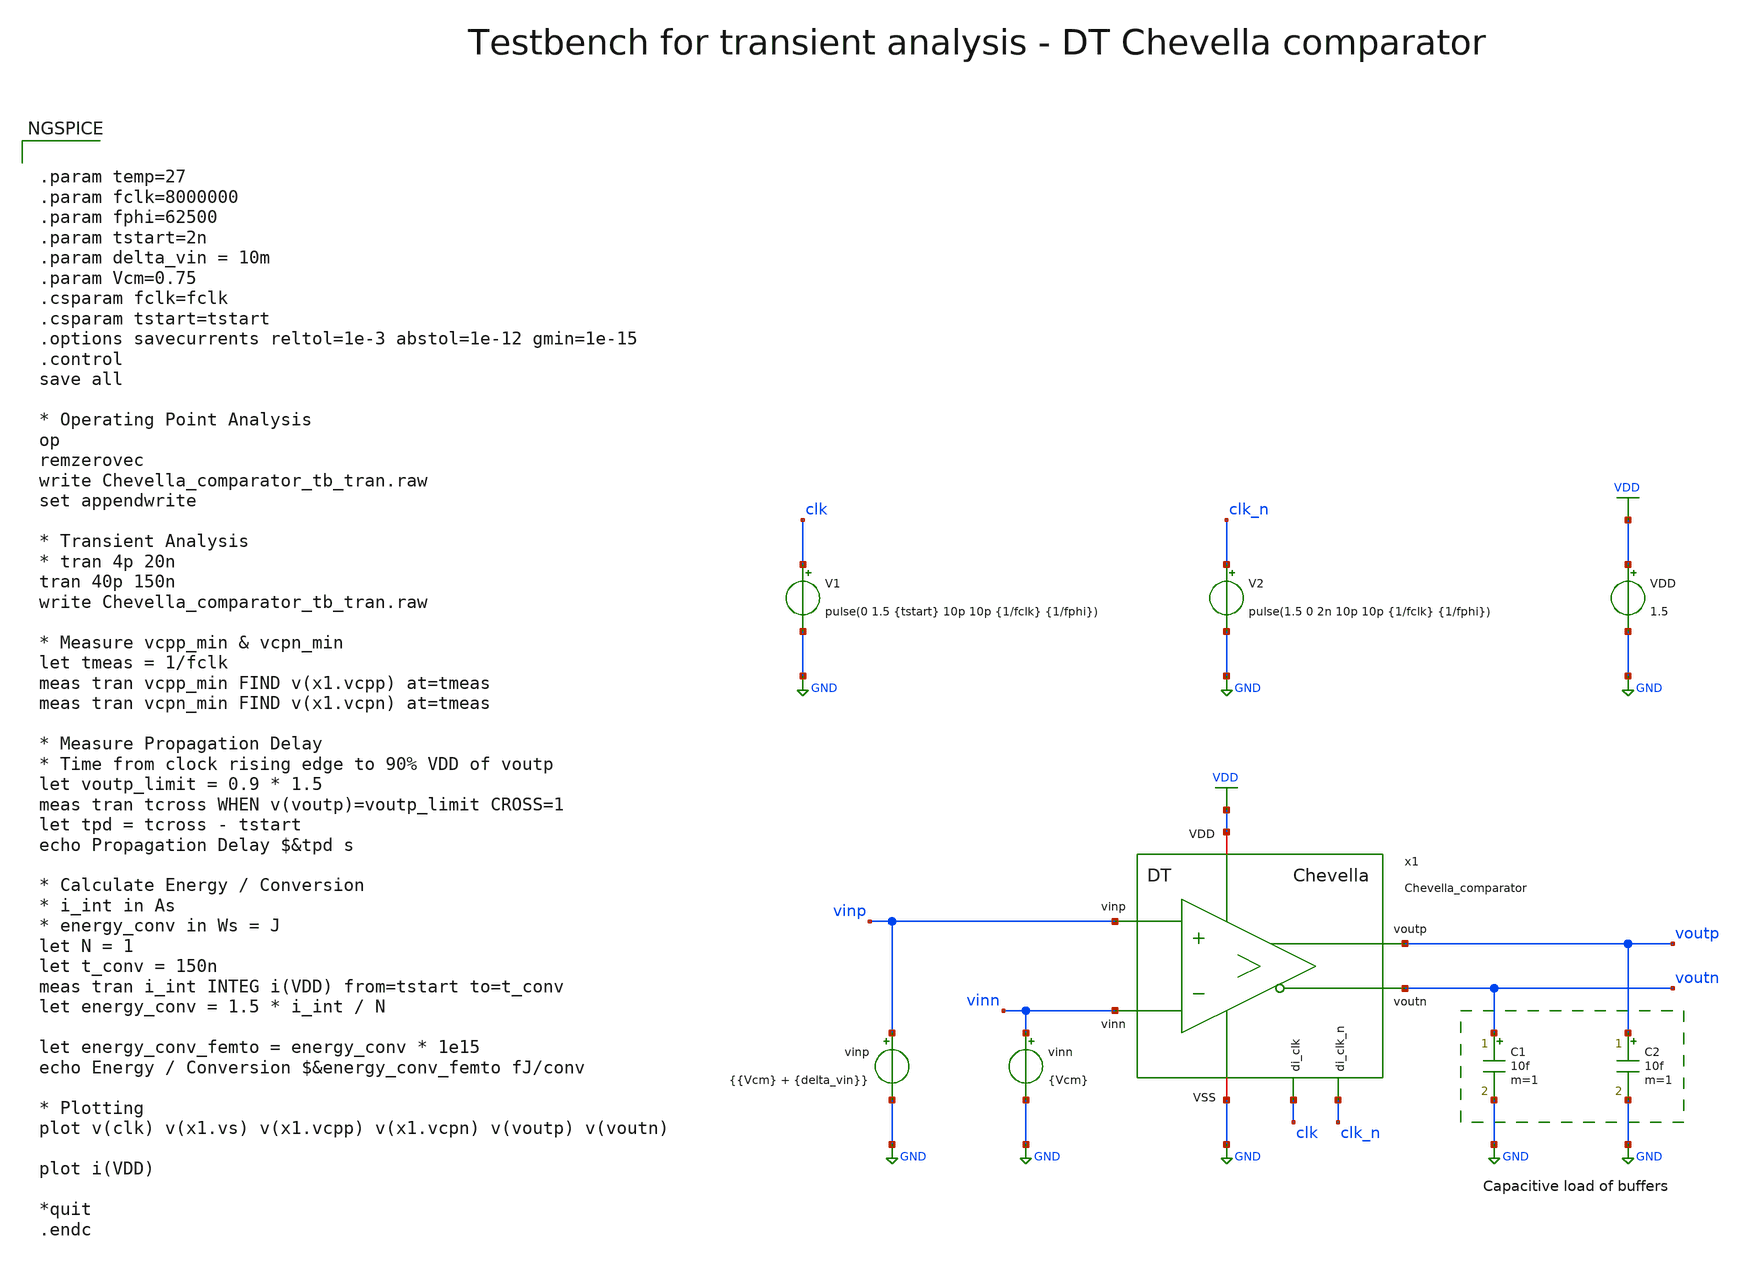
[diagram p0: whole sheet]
** sch_path: SG13G2_ATBS-ADC-main/xschem/comparator/discrete_time/Chevella/testbenches/Chevella_comparator_tb_tran.sch
**.subckt Chevella_comparator_tb_tran
VDD VDD GND 1.5
V1 clk GND pulse(0 1.5 {tstart} 10p 10p {1/fclk} {1/fphi})
vinn vinn GND {Vcm}
vinp vinp GND {{Vcm} + {delta_vin}}
V2 clk_n GND pulse(1.5 0 2n 10p 10p {1/fclk} {1/fphi})
C1 voutn GND 10f m=1
C2 voutp GND 10f m=1
x1 clk_n clk VDD voutp vinp GND voutn vinn Chevella_comparator
**** begin user architecture code

.lib cornerMOSlv.lib mos_tt
.lib cornerMOShv.lib mos_tt
.lib cornerRES.lib res_typ



.param temp=27
.param fclk=8000000
.param fphi=62500
.param tstart=2n
.param delta_vin = 10m
.param Vcm=0.75
.csparam fclk=fclk
.csparam tstart=tstart
.options savecurrents reltol=1e-3 abstol=1e-12 gmin=1e-15
.control
save all

* Operating Point Analysis
op
remzerovec
write Chevella_comparator_tb_tran.raw
set appendwrite

* Transient Analysis
* tran 4p 20n
tran 40p 150n
write Chevella_comparator_tb_tran.raw

* Measure vcpp_min & vcpn_min
let tmeas = 1/fclk
meas tran vcpp_min FIND v(x1.vcpp) at=tmeas
meas tran vcpn_min FIND v(x1.vcpn) at=tmeas

* Measure Propagation Delay
* Time from clock rising edge to 90% VDD of voutp
let voutp_limit = 0.9 * 1.5
meas tran tcross WHEN v(voutp)=voutp_limit CROSS=1
let tpd = tcross - tstart
echo Propagation Delay $&tpd s

* Calculate Energy / Conversion
* i_int in As
* energy_conv in Ws = J
let N = 1
let t_conv = 150n
meas tran i_int INTEG i(VDD) from=tstart to=t_conv
let energy_conv = 1.5 * i_int / N

let energy_conv_femto = energy_conv * 1e15
echo Energy / Conversion $&energy_conv_femto fJ/conv

* Plotting
plot v(clk) v(x1.vs) v(x1.vcpp) v(x1.vcpn) v(voutp) v(voutn)

plot i(VDD)

*quit
.endc

**** end user architecture code
**.ends

* expanding   symbol:  comparator/discrete_time/Chevella/Chevella_comparator.sym # of pins=8
** sym_path: SG13G2_ATBS-ADC-main/xschem/comparator/discrete_time/Chevella/Chevella_comparator.sym
** sch_path: SG13G2_ATBS-ADC-main/xschem/comparator/discrete_time/Chevella/Chevella_comparator.sch
.subckt Chevella_comparator di_clk_n di_clk VDD voutp vinp VSS voutn vinn
*.iopin VDD
*.opin voutp
*.opin voutn
*.ipin di_clk_n
*.iopin VSS
*.ipin vinp
*.ipin vinn
*.ipin di_clk
XM1a vcpn vinp net1 VSS sg13_lv_nmos w=1.0u l=0.13u ng=1 m=1 mm_ok=1
XM2a vcpp vinn net2 VSS sg13_lv_nmos w=1.0u l=0.13u ng=1 m=1 mm_ok=1
XM3 vs di_clk VSS VSS sg13_lv_nmos w=1.0u l=0.13u ng=1 m=1 mm_ok=1
XM4a vcpn di_clk VDD VDD sg13_lv_pmos w=1.0u l=0.13u ng=1 m=1 mm_ok=1
XM5a vcpp di_clk VDD VDD sg13_lv_pmos w=1.0u l=0.13u ng=1 m=1 mm_ok=1
XM12 voutp di_clk_n VSS VSS sg13_lv_nmos w=1.0u l=0.13u ng=1 m=1 mm_ok=1
XM8 net3 voutn VDD VDD sg13_lv_pmos w=2.0u l=0.13u ng=2 m=1 mm_ok=1
XM10 voutp voutn VSS VSS sg13_lv_nmos w=1.0u l=0.13u ng=1 m=1 mm_ok=1
XM11 voutn voutp VSS VSS sg13_lv_nmos w=1.0u l=0.13u ng=1 m=1 mm_ok=1
XM13 voutn di_clk_n VSS VSS sg13_lv_nmos w=1.0u l=0.13u ng=1 m=1 mm_ok=1
CP1 vcpn VSS 300f m=1
CP2 vcpp VSS 300f m=1
XM9 net4 voutp VDD VDD sg13_lv_pmos w=2.0u l=0.13u ng=2 m=1 mm_ok=1
XM6 voutp vcpn net3 VDD sg13_lv_pmos w=2.0u l=0.13u ng=2 m=1 mm_ok=1
XM7 voutn vcpp net4 VDD sg13_lv_pmos w=2.0u l=0.13u ng=2 m=1 mm_ok=1
XM4b net1 di_clk VDD VDD sg13_lv_pmos w=1.0u l=0.13u ng=1 m=1 mm_ok=1
XM5b net2 di_clk VDD VDD sg13_lv_pmos w=1.0u l=0.13u ng=1 m=1 mm_ok=1
XM1b net1 vcpp vs VSS sg13_lv_nmos w=1.0u l=0.13u ng=1 m=1 mm_ok=1
XM2b net2 vcpn vs VSS sg13_lv_nmos w=1.0u l=0.13u ng=1 m=1 mm_ok=1
.ends

.GLOBAL GND
.GLOBAL VDD
.end
